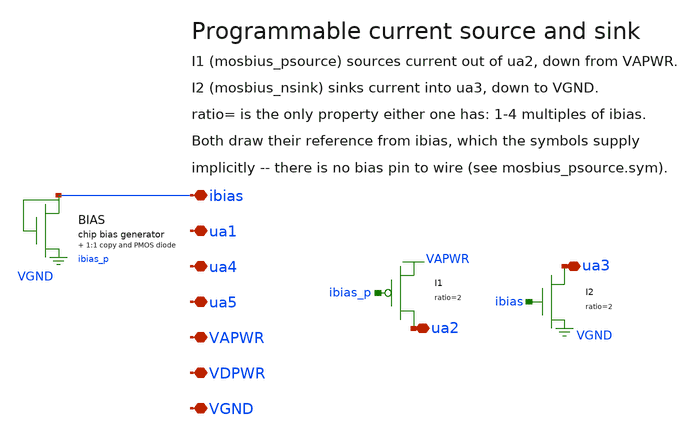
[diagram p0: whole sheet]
** sch_path: examples/currentsource/currentsource.sch
**.subckt currentsource ibias ua1 ua2 ua3 ua4 ua5 VAPWR VDPWR VGND
*.iopin ibias
*.iopin ua1
*.iopin ua2
*.iopin ua3
*.iopin ua4
*.iopin ua5
*.iopin VAPWR
*.iopin VDPWR
*.iopin VGND
XI1 ua2 ibias_p VAPWR mosbius_psource ratio=2
XI2 ua3 ibias VGND mosbius_nsink ratio=2
XBIAS ibias ibias_p VGND VAPWR mosbius_bias
**.ends

* expanding   symbol:  mosbius_psource.sym # of pins=1
** sym_path: xschem/mosbius_lib/mosbius_psource.sym
** sch_path: xschem/mosbius_lib/mosbius_psource.sch
.subckt mosbius_psource out ibias b  ratio=1
*.iopin out
XM2 out ibias b b sky130_fd_pr__pfet_g5v0d10v5 L=1 W=30*ratio nf=4*ratio ad='int((nf+1)/2) * W/nf * 0.29'
+ as='int((nf+2)/2) * W/nf * 0.29' pd='2*int((nf+1)/2) * (W/nf + 0.29)' ps='2*int((nf+2)/2) * (W/nf + 0.29)'
+ nrd='0.29 / W' nrs='0.29 / W' sa=0 sb=0 sd=0 mult=1 m=1
* implicit port ibias
* implicit port b
.ends


* expanding   symbol:  mosbius_nsink.sym # of pins=1
** sym_path: xschem/mosbius_lib/mosbius_nsink.sym
** sch_path: xschem/mosbius_lib/mosbius_nsink.sch
.subckt mosbius_nsink out ibias b  ratio=1
*.iopin out
XM2 out ibias b b sky130_fd_pr__nfet_g5v0d10v5 L=1 W=10*ratio nf=2*ratio ad='int((nf+1)/2) * W/nf * 0.29'
+ as='int((nf+2)/2) * W/nf * 0.29' pd='2*int((nf+1)/2) * (W/nf + 0.29)' ps='2*int((nf+2)/2) * (W/nf + 0.29)'
+ nrd='0.29 / W' nrs='0.29 / W' sa=0 sb=0 sd=0 mult=1 m=1
* implicit port ibias
* implicit port b
.ends


* expanding   symbol:  mosbius_bias.sym # of pins=1
** sym_path: xschem/mosbius_lib/mosbius_bias.sym
** sch_path: xschem/mosbius_lib/mosbius_bias.sch
.subckt mosbius_bias ibias ibias_p bn bp
*.iopin ibias
XMbias_ref ibias ibias bn bn sky130_fd_pr__nfet_g5v0d10v5 L=1 W=10 nf=2 ad='int((nf+1)/2) * W/nf * 0.29'
+ as='int((nf+2)/2) * W/nf * 0.29' pd='2*int((nf+1)/2) * (W/nf + 0.29)' ps='2*int((nf+2)/2) * (W/nf + 0.29)'
+ nrd='0.29 / W' nrs='0.29 / W' sa=0 sb=0 sd=0 mult=1 m=1
XMbias_copy ibias_p ibias bn bn sky130_fd_pr__nfet_g5v0d10v5 L=1 W=10 nf=2 ad='int((nf+1)/2) * W/nf * 0.29'
+ as='int((nf+2)/2) * W/nf * 0.29' pd='2*int((nf+1)/2) * (W/nf + 0.29)' ps='2*int((nf+2)/2) * (W/nf + 0.29)'
+ nrd='0.29 / W' nrs='0.29 / W' sa=0 sb=0 sd=0 mult=1 m=1
XMbias_p ibias_p ibias_p bp bp sky130_fd_pr__pfet_g5v0d10v5 L=1 W=30 nf=4 ad='int((nf+1)/2) * W/nf * 0.29'
+ as='int((nf+2)/2) * W/nf * 0.29' pd='2*int((nf+1)/2) * (W/nf + 0.29)' ps='2*int((nf+2)/2) * (W/nf + 0.29)'
+ nrd='0.29 / W' nrs='0.29 / W' sa=0 sb=0 sd=0 mult=1 m=1
* implicit port bp
.ends

.end
